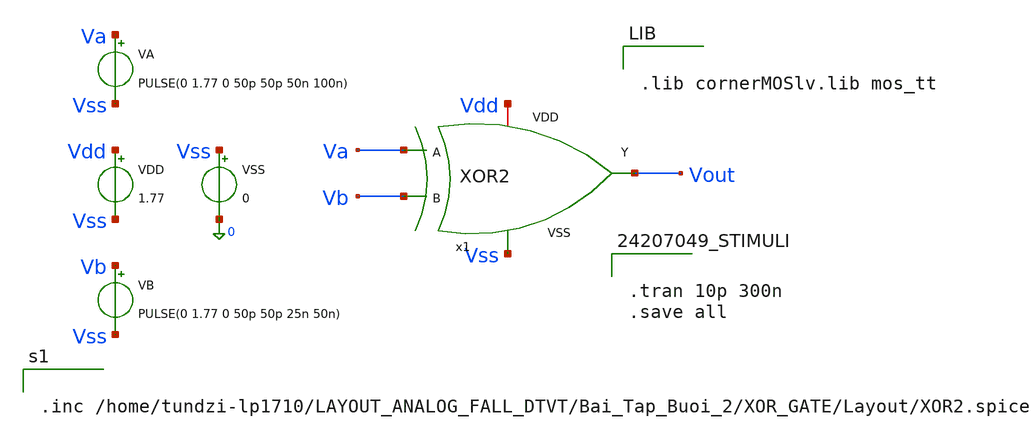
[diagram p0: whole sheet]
** sch_path: logic_gate/XOR2/LAYOUT_POST-SIMULATION/XOR2_tb.sch
**.subckt XOR2_tb
VDD Vdd Vss 1.77
VSS Vss 0 0
VA Va Vss PULSE(0 1.77 0 50p 50p 50n 100n)
VB Vb Vss PULSE(0 1.77 0 50p 50p 25n 50n)
x1 Vdd Va Vb Vss Vout XOR2
**** begin user architecture code


.lib cornerMOSlv.lib mos_tt




.tran 10p 300n
.save all




.inc /home/tundzi-lp1710/LAYOUT_ANALOG_FALL_DTVT/Bai_Tap_Buoi_2/XOR_GATE/Layout/XOR2.spice


**** end user architecture code
**.ends
.end
